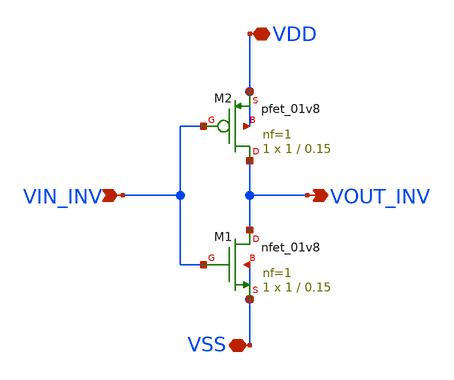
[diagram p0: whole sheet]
** sch_path: xschem/vco_inverter.sch
**.subckt vco_inverter VDD VSS VIN_INV VOUT_INV
*.iopin VDD
*.iopin VSS
*.ipin VIN_INV
*.opin VOUT_INV
XM1 VOUT_INV VIN_INV VSS VSS sky130_fd_pr__nfet_01v8 L=0.15 W=1 nf=1 ad='int((nf+1)/2) * W/nf * 0.29'
+ as='int((nf+2)/2) * W/nf * 0.29' pd='2*int((nf+1)/2) * (W/nf + 0.29)' ps='2*int((nf+2)/2) * (W/nf + 0.29)'
+ nrd='0.29 / W' nrs='0.29 / W' sa=0 sb=0 sd=0 mult=1 m=1
XM2 VOUT_INV VIN_INV VDD VDD sky130_fd_pr__pfet_01v8 L=0.15 W=1 nf=1 ad='int((nf+1)/2) * W/nf * 0.29'
+ as='int((nf+2)/2) * W/nf * 0.29' pd='2*int((nf+1)/2) * (W/nf + 0.29)' ps='2*int((nf+2)/2) * (W/nf + 0.29)'
+ nrd='0.29 / W' nrs='0.29 / W' sa=0 sb=0 sd=0 mult=1 m=1
**.ends
.end
